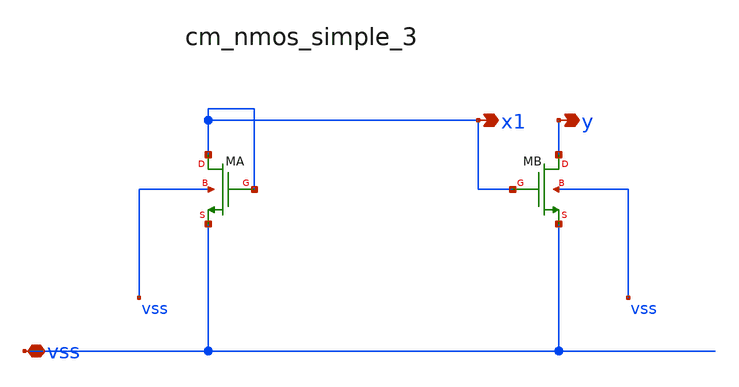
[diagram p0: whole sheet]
** sch_path: analog-db/raw/ldo_010_capless_lowiq/hier/blocks/cm_nmos_simple_3.sch
**.subckt cm_nmos_simple_3 vss x1 y
*.iopin vss
*.opin x1
*.opin y
XMA x1 x1 vss vss sg13_lv_nmos w=x_dut_xma_w l=x_dut_xma_l ng=1 m=1
XMB y x1 vss vss sg13_lv_nmos w=x_dut_xma_w l=x_dut_xma_l ng=1 m=1
**.ends
.end
